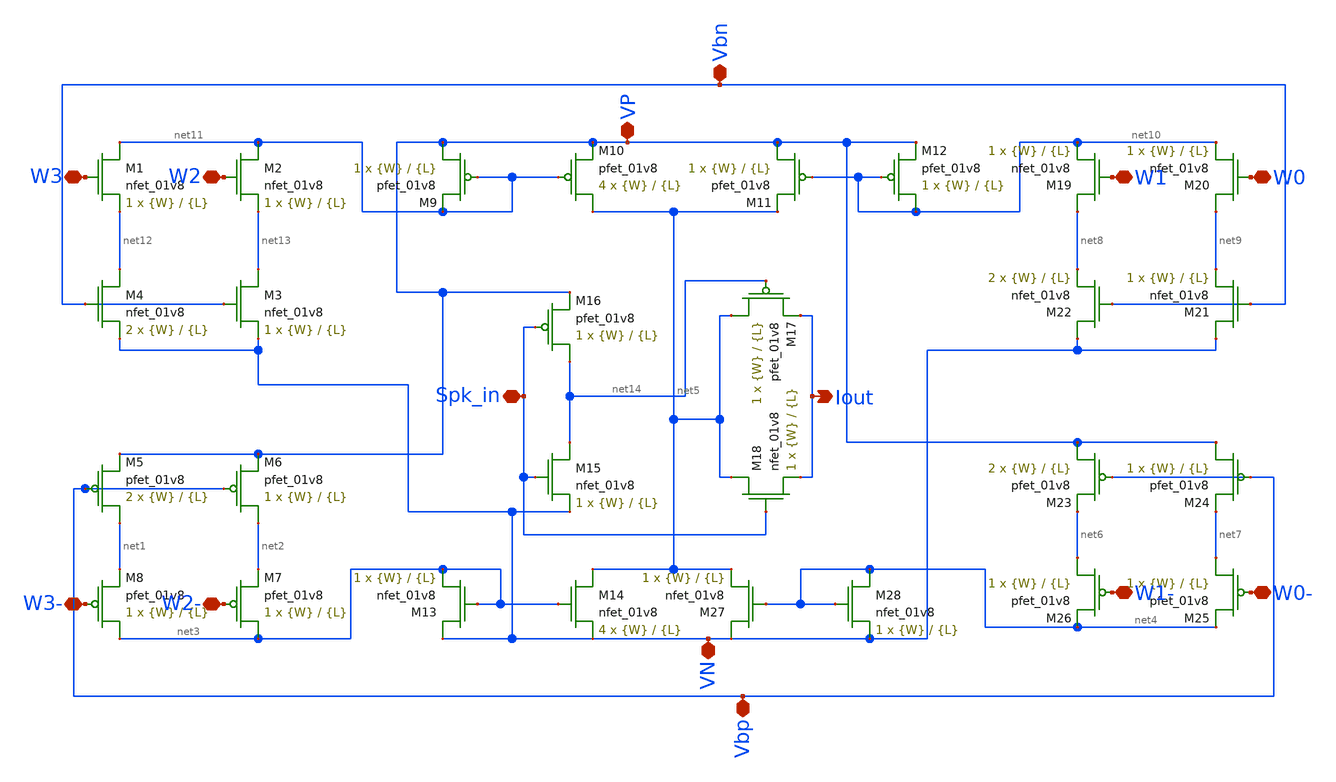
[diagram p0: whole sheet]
** sch_path: schematic/CMCI_synapse_working.sch
**.subckt CMCI_synapse_working Vbn Vbp VN VP Spk_in W3 W2 W1 W0 W0- W1- W2- W3- Iout
*.iopin Vbn
*.iopin Vbp
*.iopin VN
*.iopin VP
*.iopin Spk_in
*.iopin W3
*.iopin W2
*.iopin W1
*.iopin W0
*.iopin W0-
*.iopin W1-
*.iopin W2-
*.iopin W3-
*.opin Iout
XM1 net11 W3 net12 GND sky130_fd_pr__nfet_01v8 L={L} W={W} nf=1 ad='int((nf+1)/2) * W/nf * 0.29' as='int((nf+2)/2) * W/nf * 0.29'
+ pd='2*int((nf+1)/2) * (W/nf + 0.29)' ps='2*int((nf+2)/2) * (W/nf + 0.29)' nrd='0.29 / W' nrs='0.29 / W'
+ sa=0 sb=0 sd=0 mult=1 m=1
XM2 net11 W2 net13 GND sky130_fd_pr__nfet_01v8 L={L} W={W} nf=1 ad='int((nf+1)/2) * W/nf * 0.29' as='int((nf+2)/2) * W/nf * 0.29'
+ pd='2*int((nf+1)/2) * (W/nf + 0.29)' ps='2*int((nf+2)/2) * (W/nf + 0.29)' nrd='0.29 / W' nrs='0.29 / W'
+ sa=0 sb=0 sd=0 mult=1 m=1
XM3 net13 Vbn VN GND sky130_fd_pr__nfet_01v8 L={L} W={W} nf=1 ad='int((nf+1)/2) * W/nf * 0.29' as='int((nf+2)/2) * W/nf * 0.29'
+ pd='2*int((nf+1)/2) * (W/nf + 0.29)' ps='2*int((nf+2)/2) * (W/nf + 0.29)' nrd='0.29 / W' nrs='0.29 / W'
+ sa=0 sb=0 sd=0 mult=1 m=1
XM4 net12 Vbn VN GND sky130_fd_pr__nfet_01v8 L={L} W={W} nf=1 ad='int((nf+1)/2) * W/nf * 0.29' as='int((nf+2)/2) * W/nf * 0.29'
+ pd='2*int((nf+1)/2) * (W/nf + 0.29)' ps='2*int((nf+2)/2) * (W/nf + 0.29)' nrd='0.29 / W' nrs='0.29 / W'
+ sa=0 sb=0 sd=0 mult=2 m=2
XM5 net1 Vbp VP VDD sky130_fd_pr__pfet_01v8 L={L} W={W} nf=1 ad='int((nf+1)/2) * W/nf * 0.29' as='int((nf+2)/2) * W/nf * 0.29'
+ pd='2*int((nf+1)/2) * (W/nf + 0.29)' ps='2*int((nf+2)/2) * (W/nf + 0.29)' nrd='0.29 / W' nrs='0.29 / W'
+ sa=0 sb=0 sd=0 mult=2 m=2
XM6 net2 Vbp VP VDD sky130_fd_pr__pfet_01v8 L={L} W={W} nf=1 ad='int((nf+1)/2) * W/nf * 0.29' as='int((nf+2)/2) * W/nf * 0.29'
+ pd='2*int((nf+1)/2) * (W/nf + 0.29)' ps='2*int((nf+2)/2) * (W/nf + 0.29)' nrd='0.29 / W' nrs='0.29 / W'
+ sa=0 sb=0 sd=0 mult=1 m=1
XM7 net3 W2- net2 VDD sky130_fd_pr__pfet_01v8 L={L} W={W} nf=1 ad='int((nf+1)/2) * W/nf * 0.29' as='int((nf+2)/2) * W/nf * 0.29'
+ pd='2*int((nf+1)/2) * (W/nf + 0.29)' ps='2*int((nf+2)/2) * (W/nf + 0.29)' nrd='0.29 / W' nrs='0.29 / W'
+ sa=0 sb=0 sd=0 mult=1 m=1
XM8 net3 W3- net1 VDD sky130_fd_pr__pfet_01v8 L={L} W={W} nf=1 ad='int((nf+1)/2) * W/nf * 0.29' as='int((nf+2)/2) * W/nf * 0.29'
+ pd='2*int((nf+1)/2) * (W/nf + 0.29)' ps='2*int((nf+2)/2) * (W/nf + 0.29)' nrd='0.29 / W' nrs='0.29 / W'
+ sa=0 sb=0 sd=0 mult=1 m=1
XM9 VP net11 net11 VDD sky130_fd_pr__pfet_01v8 L={L} W={W} nf=1 ad='int((nf+1)/2) * W/nf * 0.29' as='int((nf+2)/2) * W/nf * 0.29'
+ pd='2*int((nf+1)/2) * (W/nf + 0.29)' ps='2*int((nf+2)/2) * (W/nf + 0.29)' nrd='0.29 / W' nrs='0.29 / W'
+ sa=0 sb=0 sd=0 mult=1 m=1
XM10 net5 net11 VP VDD sky130_fd_pr__pfet_01v8 L={L} W={W} nf=1 ad='int((nf+1)/2) * W/nf * 0.29' as='int((nf+2)/2) * W/nf * 0.29'
+ pd='2*int((nf+1)/2) * (W/nf + 0.29)' ps='2*int((nf+2)/2) * (W/nf + 0.29)' nrd='0.29 / W' nrs='0.29 / W'
+ sa=0 sb=0 sd=0 mult=4 m=4
XM11 VP net10 net5 VDD sky130_fd_pr__pfet_01v8 L={L} W={W} nf=1 ad='int((nf+1)/2) * W/nf * 0.29' as='int((nf+2)/2) * W/nf * 0.29'
+ pd='2*int((nf+1)/2) * (W/nf + 0.29)' ps='2*int((nf+2)/2) * (W/nf + 0.29)' nrd='0.29 / W' nrs='0.29 / W'
+ sa=0 sb=0 sd=0 mult=1 m=1
XM12 net10 net10 VP VDD sky130_fd_pr__pfet_01v8 L={L} W={W} nf=1 ad='int((nf+1)/2) * W/nf * 0.29' as='int((nf+2)/2) * W/nf * 0.29'
+ pd='2*int((nf+1)/2) * (W/nf + 0.29)' ps='2*int((nf+2)/2) * (W/nf + 0.29)' nrd='0.29 / W' nrs='0.29 / W'
+ sa=0 sb=0 sd=0 mult=1 m=1
XM13 VN net3 net3 GND sky130_fd_pr__nfet_01v8 L={L} W={W} nf=1 ad='int((nf+1)/2) * W/nf * 0.29' as='int((nf+2)/2) * W/nf * 0.29'
+ pd='2*int((nf+1)/2) * (W/nf + 0.29)' ps='2*int((nf+2)/2) * (W/nf + 0.29)' nrd='0.29 / W' nrs='0.29 / W'
+ sa=0 sb=0 sd=0 mult=1 m=1
XM14 net5 net3 VN GND sky130_fd_pr__nfet_01v8 L={L} W={W} nf=1 ad='int((nf+1)/2) * W/nf * 0.29' as='int((nf+2)/2) * W/nf * 0.29'
+ pd='2*int((nf+1)/2) * (W/nf + 0.29)' ps='2*int((nf+2)/2) * (W/nf + 0.29)' nrd='0.29 / W' nrs='0.29 / W'
+ sa=0 sb=0 sd=0 mult=4 m=4
XM15 net14 Spk_in VN GND sky130_fd_pr__nfet_01v8 L={L} W={W} nf=1 ad='int((nf+1)/2) * W/nf * 0.29' as='int((nf+2)/2) * W/nf * 0.29'
+ pd='2*int((nf+1)/2) * (W/nf + 0.29)' ps='2*int((nf+2)/2) * (W/nf + 0.29)' nrd='0.29 / W' nrs='0.29 / W'
+ sa=0 sb=0 sd=0 mult=1 m=1
XM16 net14 Spk_in VP VDD sky130_fd_pr__pfet_01v8 L={L} W={W} nf=1 ad='int((nf+1)/2) * W/nf * 0.29' as='int((nf+2)/2) * W/nf * 0.29'
+ pd='2*int((nf+1)/2) * (W/nf + 0.29)' ps='2*int((nf+2)/2) * (W/nf + 0.29)' nrd='0.29 / W' nrs='0.29 / W'
+ sa=0 sb=0 sd=0 mult=1 m=1
XM17 net5 net14 Iout VDD sky130_fd_pr__pfet_01v8 L={L} W={W} nf=1 ad='int((nf+1)/2) * W/nf * 0.29' as='int((nf+2)/2) * W/nf * 0.29'
+ pd='2*int((nf+1)/2) * (W/nf + 0.29)' ps='2*int((nf+2)/2) * (W/nf + 0.29)' nrd='0.29 / W' nrs='0.29 / W'
+ sa=0 sb=0 sd=0 mult=1 m=1
XM18 net5 Spk_in Iout GND sky130_fd_pr__nfet_01v8 L={L} W={W} nf=1 ad='int((nf+1)/2) * W/nf * 0.29' as='int((nf+2)/2) * W/nf * 0.29'
+ pd='2*int((nf+1)/2) * (W/nf + 0.29)' ps='2*int((nf+2)/2) * (W/nf + 0.29)' nrd='0.29 / W' nrs='0.29 / W'
+ sa=0 sb=0 sd=0 mult=1 m=1
XM19 net8 W1 net10 GND sky130_fd_pr__nfet_01v8 L={L} W={W} nf=1 ad='int((nf+1)/2) * W/nf * 0.29' as='int((nf+2)/2) * W/nf * 0.29'
+ pd='2*int((nf+1)/2) * (W/nf + 0.29)' ps='2*int((nf+2)/2) * (W/nf + 0.29)' nrd='0.29 / W' nrs='0.29 / W'
+ sa=0 sb=0 sd=0 mult=1 m=1
XM20 net9 W0 net10 GND sky130_fd_pr__nfet_01v8 L={L} W={W} nf=1 ad='int((nf+1)/2) * W/nf * 0.29' as='int((nf+2)/2) * W/nf * 0.29'
+ pd='2*int((nf+1)/2) * (W/nf + 0.29)' ps='2*int((nf+2)/2) * (W/nf + 0.29)' nrd='0.29 / W' nrs='0.29 / W'
+ sa=0 sb=0 sd=0 mult=1 m=1
XM21 VN Vbn net9 GND sky130_fd_pr__nfet_01v8 L={L} W={W} nf=1 ad='int((nf+1)/2) * W/nf * 0.29' as='int((nf+2)/2) * W/nf * 0.29'
+ pd='2*int((nf+1)/2) * (W/nf + 0.29)' ps='2*int((nf+2)/2) * (W/nf + 0.29)' nrd='0.29 / W' nrs='0.29 / W'
+ sa=0 sb=0 sd=0 mult=1 m=1
XM22 VN Vbn net8 GND sky130_fd_pr__nfet_01v8 L={L} W={W} nf=1 ad='int((nf+1)/2) * W/nf * 0.29' as='int((nf+2)/2) * W/nf * 0.29'
+ pd='2*int((nf+1)/2) * (W/nf + 0.29)' ps='2*int((nf+2)/2) * (W/nf + 0.29)' nrd='0.29 / W' nrs='0.29 / W'
+ sa=0 sb=0 sd=0 mult=2 m=2
XM23 VP Vbp net6 VDD sky130_fd_pr__pfet_01v8 L={L} W={W} nf=1 ad='int((nf+1)/2) * W/nf * 0.29' as='int((nf+2)/2) * W/nf * 0.29'
+ pd='2*int((nf+1)/2) * (W/nf + 0.29)' ps='2*int((nf+2)/2) * (W/nf + 0.29)' nrd='0.29 / W' nrs='0.29 / W'
+ sa=0 sb=0 sd=0 mult=2 m=2
XM24 VP Vbp net7 VDD sky130_fd_pr__pfet_01v8 L={L} W={W} nf=1 ad='int((nf+1)/2) * W/nf * 0.29' as='int((nf+2)/2) * W/nf * 0.29'
+ pd='2*int((nf+1)/2) * (W/nf + 0.29)' ps='2*int((nf+2)/2) * (W/nf + 0.29)' nrd='0.29 / W' nrs='0.29 / W'
+ sa=0 sb=0 sd=0 mult=1 m=1
XM25 net7 W0- net4 VDD sky130_fd_pr__pfet_01v8 L={L} W={W} nf=1 ad='int((nf+1)/2) * W/nf * 0.29' as='int((nf+2)/2) * W/nf * 0.29'
+ pd='2*int((nf+1)/2) * (W/nf + 0.29)' ps='2*int((nf+2)/2) * (W/nf + 0.29)' nrd='0.29 / W' nrs='0.29 / W'
+ sa=0 sb=0 sd=0 mult=1 m=1
XM26 net6 W1- net4 VDD sky130_fd_pr__pfet_01v8 L={L} W={W} nf=1 ad='int((nf+1)/2) * W/nf * 0.29' as='int((nf+2)/2) * W/nf * 0.29'
+ pd='2*int((nf+1)/2) * (W/nf + 0.29)' ps='2*int((nf+2)/2) * (W/nf + 0.29)' nrd='0.29 / W' nrs='0.29 / W'
+ sa=0 sb=0 sd=0 mult=1 m=1
XM27 VN net4 net5 GND sky130_fd_pr__nfet_01v8 L={L} W={W} nf=1 ad='int((nf+1)/2) * W/nf * 0.29' as='int((nf+2)/2) * W/nf * 0.29'
+ pd='2*int((nf+1)/2) * (W/nf + 0.29)' ps='2*int((nf+2)/2) * (W/nf + 0.29)' nrd='0.29 / W' nrs='0.29 / W'
+ sa=0 sb=0 sd=0 mult=1 m=1
XM28 net4 net4 VN GND sky130_fd_pr__nfet_01v8 L={L} W={W} nf=1 ad='int((nf+1)/2) * W/nf * 0.29' as='int((nf+2)/2) * W/nf * 0.29'
+ pd='2*int((nf+1)/2) * (W/nf + 0.29)' ps='2*int((nf+2)/2) * (W/nf + 0.29)' nrd='0.29 / W' nrs='0.29 / W'
+ sa=0 sb=0 sd=0 mult=1 m=1
**.ends
.end
